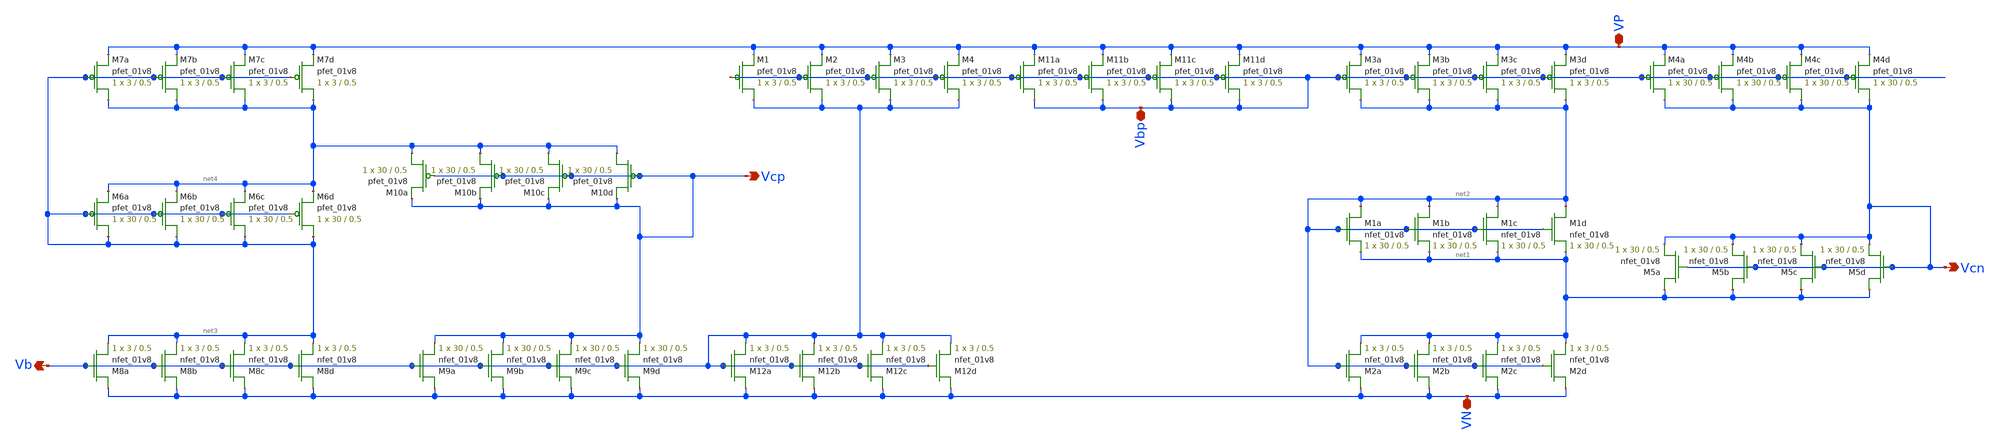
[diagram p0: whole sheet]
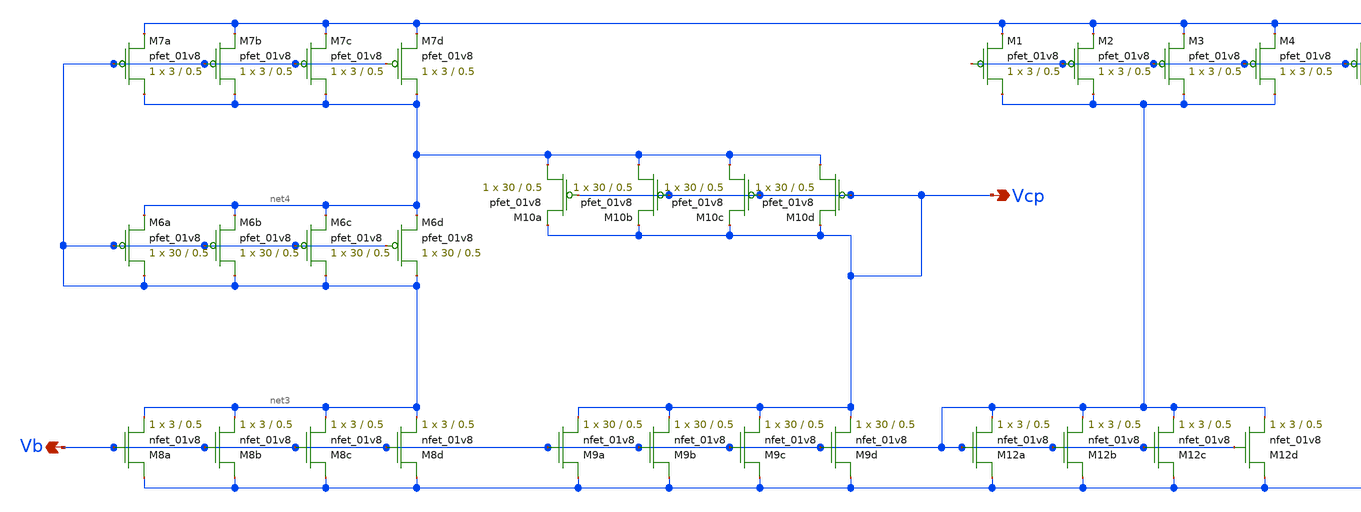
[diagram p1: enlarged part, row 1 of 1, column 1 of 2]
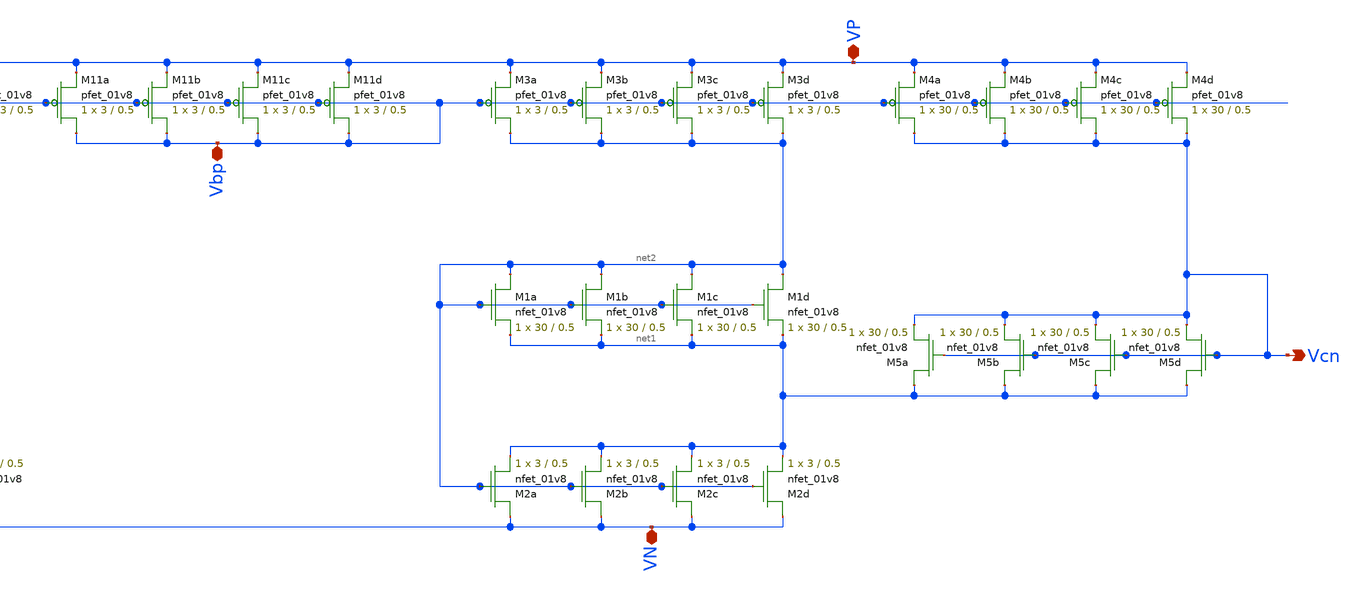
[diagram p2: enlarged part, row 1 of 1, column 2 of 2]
** sch_path: mp3/xschem/bias_schematic.sch
**.subckt bias_schematic VP VN Vcp Vbp Vcn Vb
*.iopin VP
*.iopin VN
*.opin Vcp
*.iopin Vbp
*.opin Vcn
*.opin Vb
XM1a net2 net2 net1 GND sky130_fd_pr__nfet_01v8 L=0.5 W=30 nf=1 ad='int((nf+1)/2) * W/nf * 0.29' as='int((nf+2)/2) * W/nf * 0.29'
+ pd='2*int((nf+1)/2) * (W/nf + 0.29)' ps='2*int((nf+2)/2) * (W/nf + 0.29)' nrd='0.29 / W' nrs='0.29 / W'
+ sa=0 sb=0 sd=0 mult=1 m=1
XM1b net2 net2 net1 GND sky130_fd_pr__nfet_01v8 L=0.5 W=30 nf=1 ad='int((nf+1)/2) * W/nf * 0.29' as='int((nf+2)/2) * W/nf * 0.29'
+ pd='2*int((nf+1)/2) * (W/nf + 0.29)' ps='2*int((nf+2)/2) * (W/nf + 0.29)' nrd='0.29 / W' nrs='0.29 / W'
+ sa=0 sb=0 sd=0 mult=1 m=1
XM1c net2 net2 net1 GND sky130_fd_pr__nfet_01v8 L=0.5 W=30 nf=1 ad='int((nf+1)/2) * W/nf * 0.29' as='int((nf+2)/2) * W/nf * 0.29'
+ pd='2*int((nf+1)/2) * (W/nf + 0.29)' ps='2*int((nf+2)/2) * (W/nf + 0.29)' nrd='0.29 / W' nrs='0.29 / W'
+ sa=0 sb=0 sd=0 mult=1 m=1
XM1d net2 net2 net1 GND sky130_fd_pr__nfet_01v8 L=0.5 W=30 nf=1 ad='int((nf+1)/2) * W/nf * 0.29' as='int((nf+2)/2) * W/nf * 0.29'
+ pd='2*int((nf+1)/2) * (W/nf + 0.29)' ps='2*int((nf+2)/2) * (W/nf + 0.29)' nrd='0.29 / W' nrs='0.29 / W'
+ sa=0 sb=0 sd=0 mult=1 m=1
XM2a VN net2 net1 GND sky130_fd_pr__nfet_01v8 L=0.5 W=3 nf=1 ad='int((nf+1)/2) * W/nf * 0.29' as='int((nf+2)/2) * W/nf * 0.29'
+ pd='2*int((nf+1)/2) * (W/nf + 0.29)' ps='2*int((nf+2)/2) * (W/nf + 0.29)' nrd='0.29 / W' nrs='0.29 / W'
+ sa=0 sb=0 sd=0 mult=1 m=1
XM2b VN net2 net1 GND sky130_fd_pr__nfet_01v8 L=0.5 W=3 nf=1 ad='int((nf+1)/2) * W/nf * 0.29' as='int((nf+2)/2) * W/nf * 0.29'
+ pd='2*int((nf+1)/2) * (W/nf + 0.29)' ps='2*int((nf+2)/2) * (W/nf + 0.29)' nrd='0.29 / W' nrs='0.29 / W'
+ sa=0 sb=0 sd=0 mult=1 m=1
XM2c VN net2 net1 GND sky130_fd_pr__nfet_01v8 L=0.5 W=3 nf=1 ad='int((nf+1)/2) * W/nf * 0.29' as='int((nf+2)/2) * W/nf * 0.29'
+ pd='2*int((nf+1)/2) * (W/nf + 0.29)' ps='2*int((nf+2)/2) * (W/nf + 0.29)' nrd='0.29 / W' nrs='0.29 / W'
+ sa=0 sb=0 sd=0 mult=1 m=1
XM2d VN net2 net1 GND sky130_fd_pr__nfet_01v8 L=0.5 W=3 nf=1 ad='int((nf+1)/2) * W/nf * 0.29' as='int((nf+2)/2) * W/nf * 0.29'
+ pd='2*int((nf+1)/2) * (W/nf + 0.29)' ps='2*int((nf+2)/2) * (W/nf + 0.29)' nrd='0.29 / W' nrs='0.29 / W'
+ sa=0 sb=0 sd=0 mult=1 m=1
XM3a net2 Vbp VP VDD sky130_fd_pr__pfet_01v8 L=0.5 W=3 nf=1 ad='int((nf+1)/2) * W/nf * 0.29' as='int((nf+2)/2) * W/nf * 0.29'
+ pd='2*int((nf+1)/2) * (W/nf + 0.29)' ps='2*int((nf+2)/2) * (W/nf + 0.29)' nrd='0.29 / W' nrs='0.29 / W'
+ sa=0 sb=0 sd=0 mult=1 m=1
XM3b net2 Vbp VP VDD sky130_fd_pr__pfet_01v8 L=0.5 W=3 nf=1 ad='int((nf+1)/2) * W/nf * 0.29' as='int((nf+2)/2) * W/nf * 0.29'
+ pd='2*int((nf+1)/2) * (W/nf + 0.29)' ps='2*int((nf+2)/2) * (W/nf + 0.29)' nrd='0.29 / W' nrs='0.29 / W'
+ sa=0 sb=0 sd=0 mult=1 m=1
XM3c net2 Vbp VP VDD sky130_fd_pr__pfet_01v8 L=0.5 W=3 nf=1 ad='int((nf+1)/2) * W/nf * 0.29' as='int((nf+2)/2) * W/nf * 0.29'
+ pd='2*int((nf+1)/2) * (W/nf + 0.29)' ps='2*int((nf+2)/2) * (W/nf + 0.29)' nrd='0.29 / W' nrs='0.29 / W'
+ sa=0 sb=0 sd=0 mult=1 m=1
XM3d net2 Vbp VP VDD sky130_fd_pr__pfet_01v8 L=0.5 W=3 nf=1 ad='int((nf+1)/2) * W/nf * 0.29' as='int((nf+2)/2) * W/nf * 0.29'
+ pd='2*int((nf+1)/2) * (W/nf + 0.29)' ps='2*int((nf+2)/2) * (W/nf + 0.29)' nrd='0.29 / W' nrs='0.29 / W'
+ sa=0 sb=0 sd=0 mult=1 m=1
XM4a Vcn Vbp VP VDD sky130_fd_pr__pfet_01v8 L=0.5 W=30 nf=1 ad='int((nf+1)/2) * W/nf * 0.29' as='int((nf+2)/2) * W/nf * 0.29'
+ pd='2*int((nf+1)/2) * (W/nf + 0.29)' ps='2*int((nf+2)/2) * (W/nf + 0.29)' nrd='0.29 / W' nrs='0.29 / W'
+ sa=0 sb=0 sd=0 mult=1 m=1
XM4b Vcn Vbp VP VDD sky130_fd_pr__pfet_01v8 L=0.5 W=30 nf=1 ad='int((nf+1)/2) * W/nf * 0.29' as='int((nf+2)/2) * W/nf * 0.29'
+ pd='2*int((nf+1)/2) * (W/nf + 0.29)' ps='2*int((nf+2)/2) * (W/nf + 0.29)' nrd='0.29 / W' nrs='0.29 / W'
+ sa=0 sb=0 sd=0 mult=1 m=1
XM4c Vcn Vbp VP VDD sky130_fd_pr__pfet_01v8 L=0.5 W=30 nf=1 ad='int((nf+1)/2) * W/nf * 0.29' as='int((nf+2)/2) * W/nf * 0.29'
+ pd='2*int((nf+1)/2) * (W/nf + 0.29)' ps='2*int((nf+2)/2) * (W/nf + 0.29)' nrd='0.29 / W' nrs='0.29 / W'
+ sa=0 sb=0 sd=0 mult=1 m=1
XM4d Vcn Vbp VP VDD sky130_fd_pr__pfet_01v8 L=0.5 W=30 nf=1 ad='int((nf+1)/2) * W/nf * 0.29' as='int((nf+2)/2) * W/nf * 0.29'
+ pd='2*int((nf+1)/2) * (W/nf + 0.29)' ps='2*int((nf+2)/2) * (W/nf + 0.29)' nrd='0.29 / W' nrs='0.29 / W'
+ sa=0 sb=0 sd=0 mult=1 m=1
XM11a Vbp Vbp VP VDD sky130_fd_pr__pfet_01v8 L=0.5 W=3 nf=1 ad='int((nf+1)/2) * W/nf * 0.29' as='int((nf+2)/2) * W/nf * 0.29'
+ pd='2*int((nf+1)/2) * (W/nf + 0.29)' ps='2*int((nf+2)/2) * (W/nf + 0.29)' nrd='0.29 / W' nrs='0.29 / W'
+ sa=0 sb=0 sd=0 mult=1 m=1
XM11b Vbp Vbp VP VDD sky130_fd_pr__pfet_01v8 L=0.5 W=3 nf=1 ad='int((nf+1)/2) * W/nf * 0.29' as='int((nf+2)/2) * W/nf * 0.29'
+ pd='2*int((nf+1)/2) * (W/nf + 0.29)' ps='2*int((nf+2)/2) * (W/nf + 0.29)' nrd='0.29 / W' nrs='0.29 / W'
+ sa=0 sb=0 sd=0 mult=1 m=1
XM11c Vbp Vbp VP VDD sky130_fd_pr__pfet_01v8 L=0.5 W=3 nf=1 ad='int((nf+1)/2) * W/nf * 0.29' as='int((nf+2)/2) * W/nf * 0.29'
+ pd='2*int((nf+1)/2) * (W/nf + 0.29)' ps='2*int((nf+2)/2) * (W/nf + 0.29)' nrd='0.29 / W' nrs='0.29 / W'
+ sa=0 sb=0 sd=0 mult=1 m=1
XM11d Vbp Vbp VP VDD sky130_fd_pr__pfet_01v8 L=0.5 W=3 nf=1 ad='int((nf+1)/2) * W/nf * 0.29' as='int((nf+2)/2) * W/nf * 0.29'
+ pd='2*int((nf+1)/2) * (W/nf + 0.29)' ps='2*int((nf+2)/2) * (W/nf + 0.29)' nrd='0.29 / W' nrs='0.29 / W'
+ sa=0 sb=0 sd=0 mult=1 m=1
XM5a net1 Vcn Vcn GND sky130_fd_pr__nfet_01v8 L=0.5 W=30 nf=1 ad='int((nf+1)/2) * W/nf * 0.29' as='int((nf+2)/2) * W/nf * 0.29'
+ pd='2*int((nf+1)/2) * (W/nf + 0.29)' ps='2*int((nf+2)/2) * (W/nf + 0.29)' nrd='0.29 / W' nrs='0.29 / W'
+ sa=0 sb=0 sd=0 mult=1 m=1
XM5b net1 Vcn Vcn GND sky130_fd_pr__nfet_01v8 L=0.5 W=30 nf=1 ad='int((nf+1)/2) * W/nf * 0.29' as='int((nf+2)/2) * W/nf * 0.29'
+ pd='2*int((nf+1)/2) * (W/nf + 0.29)' ps='2*int((nf+2)/2) * (W/nf + 0.29)' nrd='0.29 / W' nrs='0.29 / W'
+ sa=0 sb=0 sd=0 mult=1 m=1
XM5c net1 Vcn Vcn GND sky130_fd_pr__nfet_01v8 L=0.5 W=30 nf=1 ad='int((nf+1)/2) * W/nf * 0.29' as='int((nf+2)/2) * W/nf * 0.29'
+ pd='2*int((nf+1)/2) * (W/nf + 0.29)' ps='2*int((nf+2)/2) * (W/nf + 0.29)' nrd='0.29 / W' nrs='0.29 / W'
+ sa=0 sb=0 sd=0 mult=1 m=1
XM5d net1 Vcn Vcn GND sky130_fd_pr__nfet_01v8 L=0.5 W=30 nf=1 ad='int((nf+1)/2) * W/nf * 0.29' as='int((nf+2)/2) * W/nf * 0.29'
+ pd='2*int((nf+1)/2) * (W/nf + 0.29)' ps='2*int((nf+2)/2) * (W/nf + 0.29)' nrd='0.29 / W' nrs='0.29 / W'
+ sa=0 sb=0 sd=0 mult=1 m=1
XM8a VN Vb net3 GND sky130_fd_pr__nfet_01v8 L=0.5 W=3 nf=1 ad='int((nf+1)/2) * W/nf * 0.29' as='int((nf+2)/2) * W/nf * 0.29'
+ pd='2*int((nf+1)/2) * (W/nf + 0.29)' ps='2*int((nf+2)/2) * (W/nf + 0.29)' nrd='0.29 / W' nrs='0.29 / W'
+ sa=0 sb=0 sd=0 mult=1 m=1
XM8b VN Vb net3 GND sky130_fd_pr__nfet_01v8 L=0.5 W=3 nf=1 ad='int((nf+1)/2) * W/nf * 0.29' as='int((nf+2)/2) * W/nf * 0.29'
+ pd='2*int((nf+1)/2) * (W/nf + 0.29)' ps='2*int((nf+2)/2) * (W/nf + 0.29)' nrd='0.29 / W' nrs='0.29 / W'
+ sa=0 sb=0 sd=0 mult=1 m=1
XM8c VN Vb net3 GND sky130_fd_pr__nfet_01v8 L=0.5 W=3 nf=1 ad='int((nf+1)/2) * W/nf * 0.29' as='int((nf+2)/2) * W/nf * 0.29'
+ pd='2*int((nf+1)/2) * (W/nf + 0.29)' ps='2*int((nf+2)/2) * (W/nf + 0.29)' nrd='0.29 / W' nrs='0.29 / W'
+ sa=0 sb=0 sd=0 mult=1 m=1
XM8d VN Vb net3 GND sky130_fd_pr__nfet_01v8 L=0.5 W=3 nf=1 ad='int((nf+1)/2) * W/nf * 0.29' as='int((nf+2)/2) * W/nf * 0.29'
+ pd='2*int((nf+1)/2) * (W/nf + 0.29)' ps='2*int((nf+2)/2) * (W/nf + 0.29)' nrd='0.29 / W' nrs='0.29 / W'
+ sa=0 sb=0 sd=0 mult=1 m=1
XM6a net3 net3 net4 VDD sky130_fd_pr__pfet_01v8 L=0.5 W=30 nf=1 ad='int((nf+1)/2) * W/nf * 0.29' as='int((nf+2)/2) * W/nf * 0.29'
+ pd='2*int((nf+1)/2) * (W/nf + 0.29)' ps='2*int((nf+2)/2) * (W/nf + 0.29)' nrd='0.29 / W' nrs='0.29 / W'
+ sa=0 sb=0 sd=0 mult=1 m=1
XM6b net3 net3 net4 VDD sky130_fd_pr__pfet_01v8 L=0.5 W=30 nf=1 ad='int((nf+1)/2) * W/nf * 0.29' as='int((nf+2)/2) * W/nf * 0.29'
+ pd='2*int((nf+1)/2) * (W/nf + 0.29)' ps='2*int((nf+2)/2) * (W/nf + 0.29)' nrd='0.29 / W' nrs='0.29 / W'
+ sa=0 sb=0 sd=0 mult=1 m=1
XM6c net3 net3 net4 VDD sky130_fd_pr__pfet_01v8 L=0.5 W=30 nf=1 ad='int((nf+1)/2) * W/nf * 0.29' as='int((nf+2)/2) * W/nf * 0.29'
+ pd='2*int((nf+1)/2) * (W/nf + 0.29)' ps='2*int((nf+2)/2) * (W/nf + 0.29)' nrd='0.29 / W' nrs='0.29 / W'
+ sa=0 sb=0 sd=0 mult=1 m=1
XM6d net3 net3 net4 VDD sky130_fd_pr__pfet_01v8 L=0.5 W=30 nf=1 ad='int((nf+1)/2) * W/nf * 0.29' as='int((nf+2)/2) * W/nf * 0.29'
+ pd='2*int((nf+1)/2) * (W/nf + 0.29)' ps='2*int((nf+2)/2) * (W/nf + 0.29)' nrd='0.29 / W' nrs='0.29 / W'
+ sa=0 sb=0 sd=0 mult=1 m=1
XM7a net4 net3 VP VDD sky130_fd_pr__pfet_01v8 L=0.5 W=3 nf=1 ad='int((nf+1)/2) * W/nf * 0.29' as='int((nf+2)/2) * W/nf * 0.29'
+ pd='2*int((nf+1)/2) * (W/nf + 0.29)' ps='2*int((nf+2)/2) * (W/nf + 0.29)' nrd='0.29 / W' nrs='0.29 / W'
+ sa=0 sb=0 sd=0 mult=1 m=1
XM7b net4 net3 VP VDD sky130_fd_pr__pfet_01v8 L=0.5 W=3 nf=1 ad='int((nf+1)/2) * W/nf * 0.29' as='int((nf+2)/2) * W/nf * 0.29'
+ pd='2*int((nf+1)/2) * (W/nf + 0.29)' ps='2*int((nf+2)/2) * (W/nf + 0.29)' nrd='0.29 / W' nrs='0.29 / W'
+ sa=0 sb=0 sd=0 mult=1 m=1
XM7c net4 net3 VP VDD sky130_fd_pr__pfet_01v8 L=0.5 W=3 nf=1 ad='int((nf+1)/2) * W/nf * 0.29' as='int((nf+2)/2) * W/nf * 0.29'
+ pd='2*int((nf+1)/2) * (W/nf + 0.29)' ps='2*int((nf+2)/2) * (W/nf + 0.29)' nrd='0.29 / W' nrs='0.29 / W'
+ sa=0 sb=0 sd=0 mult=1 m=1
XM7d net4 net3 VP VDD sky130_fd_pr__pfet_01v8 L=0.5 W=3 nf=1 ad='int((nf+1)/2) * W/nf * 0.29' as='int((nf+2)/2) * W/nf * 0.29'
+ pd='2*int((nf+1)/2) * (W/nf + 0.29)' ps='2*int((nf+2)/2) * (W/nf + 0.29)' nrd='0.29 / W' nrs='0.29 / W'
+ sa=0 sb=0 sd=0 mult=1 m=1
XM10d net4 Vcp Vcp VDD sky130_fd_pr__pfet_01v8 L=0.5 W=30 nf=1 ad='int((nf+1)/2) * W/nf * 0.29' as='int((nf+2)/2) * W/nf * 0.29'
+ pd='2*int((nf+1)/2) * (W/nf + 0.29)' ps='2*int((nf+2)/2) * (W/nf + 0.29)' nrd='0.29 / W' nrs='0.29 / W'
+ sa=0 sb=0 sd=0 mult=1 m=1
XM10c net4 Vcp Vcp VDD sky130_fd_pr__pfet_01v8 L=0.5 W=30 nf=1 ad='int((nf+1)/2) * W/nf * 0.29' as='int((nf+2)/2) * W/nf * 0.29'
+ pd='2*int((nf+1)/2) * (W/nf + 0.29)' ps='2*int((nf+2)/2) * (W/nf + 0.29)' nrd='0.29 / W' nrs='0.29 / W'
+ sa=0 sb=0 sd=0 mult=1 m=1
XM10b net4 Vcp Vcp VDD sky130_fd_pr__pfet_01v8 L=0.5 W=30 nf=1 ad='int((nf+1)/2) * W/nf * 0.29' as='int((nf+2)/2) * W/nf * 0.29'
+ pd='2*int((nf+1)/2) * (W/nf + 0.29)' ps='2*int((nf+2)/2) * (W/nf + 0.29)' nrd='0.29 / W' nrs='0.29 / W'
+ sa=0 sb=0 sd=0 mult=1 m=1
XM10a net4 Vcp Vcp VDD sky130_fd_pr__pfet_01v8 L=0.5 W=30 nf=1 ad='int((nf+1)/2) * W/nf * 0.29' as='int((nf+2)/2) * W/nf * 0.29'
+ pd='2*int((nf+1)/2) * (W/nf + 0.29)' ps='2*int((nf+2)/2) * (W/nf + 0.29)' nrd='0.29 / W' nrs='0.29 / W'
+ sa=0 sb=0 sd=0 mult=1 m=1
XM9a VN Vb Vcp GND sky130_fd_pr__nfet_01v8 L=0.5 W=30 nf=1 ad='int((nf+1)/2) * W/nf * 0.29' as='int((nf+2)/2) * W/nf * 0.29'
+ pd='2*int((nf+1)/2) * (W/nf + 0.29)' ps='2*int((nf+2)/2) * (W/nf + 0.29)' nrd='0.29 / W' nrs='0.29 / W'
+ sa=0 sb=0 sd=0 mult=1 m=1
XM9b VN Vb Vcp GND sky130_fd_pr__nfet_01v8 L=0.5 W=30 nf=1 ad='int((nf+1)/2) * W/nf * 0.29' as='int((nf+2)/2) * W/nf * 0.29'
+ pd='2*int((nf+1)/2) * (W/nf + 0.29)' ps='2*int((nf+2)/2) * (W/nf + 0.29)' nrd='0.29 / W' nrs='0.29 / W'
+ sa=0 sb=0 sd=0 mult=1 m=1
XM9c VN Vb Vcp GND sky130_fd_pr__nfet_01v8 L=0.5 W=30 nf=1 ad='int((nf+1)/2) * W/nf * 0.29' as='int((nf+2)/2) * W/nf * 0.29'
+ pd='2*int((nf+1)/2) * (W/nf + 0.29)' ps='2*int((nf+2)/2) * (W/nf + 0.29)' nrd='0.29 / W' nrs='0.29 / W'
+ sa=0 sb=0 sd=0 mult=1 m=1
XM9d VN Vb Vcp GND sky130_fd_pr__nfet_01v8 L=0.5 W=30 nf=1 ad='int((nf+1)/2) * W/nf * 0.29' as='int((nf+2)/2) * W/nf * 0.29'
+ pd='2*int((nf+1)/2) * (W/nf + 0.29)' ps='2*int((nf+2)/2) * (W/nf + 0.29)' nrd='0.29 / W' nrs='0.29 / W'
+ sa=0 sb=0 sd=0 mult=1 m=1
XM12a VN Vb Vb GND sky130_fd_pr__nfet_01v8 L=0.5 W=3 nf=1 ad='int((nf+1)/2) * W/nf * 0.29' as='int((nf+2)/2) * W/nf * 0.29'
+ pd='2*int((nf+1)/2) * (W/nf + 0.29)' ps='2*int((nf+2)/2) * (W/nf + 0.29)' nrd='0.29 / W' nrs='0.29 / W'
+ sa=0 sb=0 sd=0 mult=1 m=1
XM12b VN Vb Vb GND sky130_fd_pr__nfet_01v8 L=0.5 W=3 nf=1 ad='int((nf+1)/2) * W/nf * 0.29' as='int((nf+2)/2) * W/nf * 0.29'
+ pd='2*int((nf+1)/2) * (W/nf + 0.29)' ps='2*int((nf+2)/2) * (W/nf + 0.29)' nrd='0.29 / W' nrs='0.29 / W'
+ sa=0 sb=0 sd=0 mult=1 m=1
XM12c VN Vb Vb GND sky130_fd_pr__nfet_01v8 L=0.5 W=3 nf=1 ad='int((nf+1)/2) * W/nf * 0.29' as='int((nf+2)/2) * W/nf * 0.29'
+ pd='2*int((nf+1)/2) * (W/nf + 0.29)' ps='2*int((nf+2)/2) * (W/nf + 0.29)' nrd='0.29 / W' nrs='0.29 / W'
+ sa=0 sb=0 sd=0 mult=1 m=1
XM12d VN Vb Vb GND sky130_fd_pr__nfet_01v8 L=0.5 W=3 nf=1 ad='int((nf+1)/2) * W/nf * 0.29' as='int((nf+2)/2) * W/nf * 0.29'
+ pd='2*int((nf+1)/2) * (W/nf + 0.29)' ps='2*int((nf+2)/2) * (W/nf + 0.29)' nrd='0.29 / W' nrs='0.29 / W'
+ sa=0 sb=0 sd=0 mult=1 m=1
XM1 Vb Vbp VP VDD sky130_fd_pr__pfet_01v8 L=0.5 W=3 nf=1 ad='int((nf+1)/2) * W/nf * 0.29' as='int((nf+2)/2) * W/nf * 0.29'
+ pd='2*int((nf+1)/2) * (W/nf + 0.29)' ps='2*int((nf+2)/2) * (W/nf + 0.29)' nrd='0.29 / W' nrs='0.29 / W'
+ sa=0 sb=0 sd=0 mult=1 m=1
XM2 Vb Vbp VP VDD sky130_fd_pr__pfet_01v8 L=0.5 W=3 nf=1 ad='int((nf+1)/2) * W/nf * 0.29' as='int((nf+2)/2) * W/nf * 0.29'
+ pd='2*int((nf+1)/2) * (W/nf + 0.29)' ps='2*int((nf+2)/2) * (W/nf + 0.29)' nrd='0.29 / W' nrs='0.29 / W'
+ sa=0 sb=0 sd=0 mult=1 m=1
XM3 Vb Vbp VP VDD sky130_fd_pr__pfet_01v8 L=0.5 W=3 nf=1 ad='int((nf+1)/2) * W/nf * 0.29' as='int((nf+2)/2) * W/nf * 0.29'
+ pd='2*int((nf+1)/2) * (W/nf + 0.29)' ps='2*int((nf+2)/2) * (W/nf + 0.29)' nrd='0.29 / W' nrs='0.29 / W'
+ sa=0 sb=0 sd=0 mult=1 m=1
XM4 Vb Vbp VP VDD sky130_fd_pr__pfet_01v8 L=0.5 W=3 nf=1 ad='int((nf+1)/2) * W/nf * 0.29' as='int((nf+2)/2) * W/nf * 0.29'
+ pd='2*int((nf+1)/2) * (W/nf + 0.29)' ps='2*int((nf+2)/2) * (W/nf + 0.29)' nrd='0.29 / W' nrs='0.29 / W'
+ sa=0 sb=0 sd=0 mult=1 m=1
**.ends
.end
